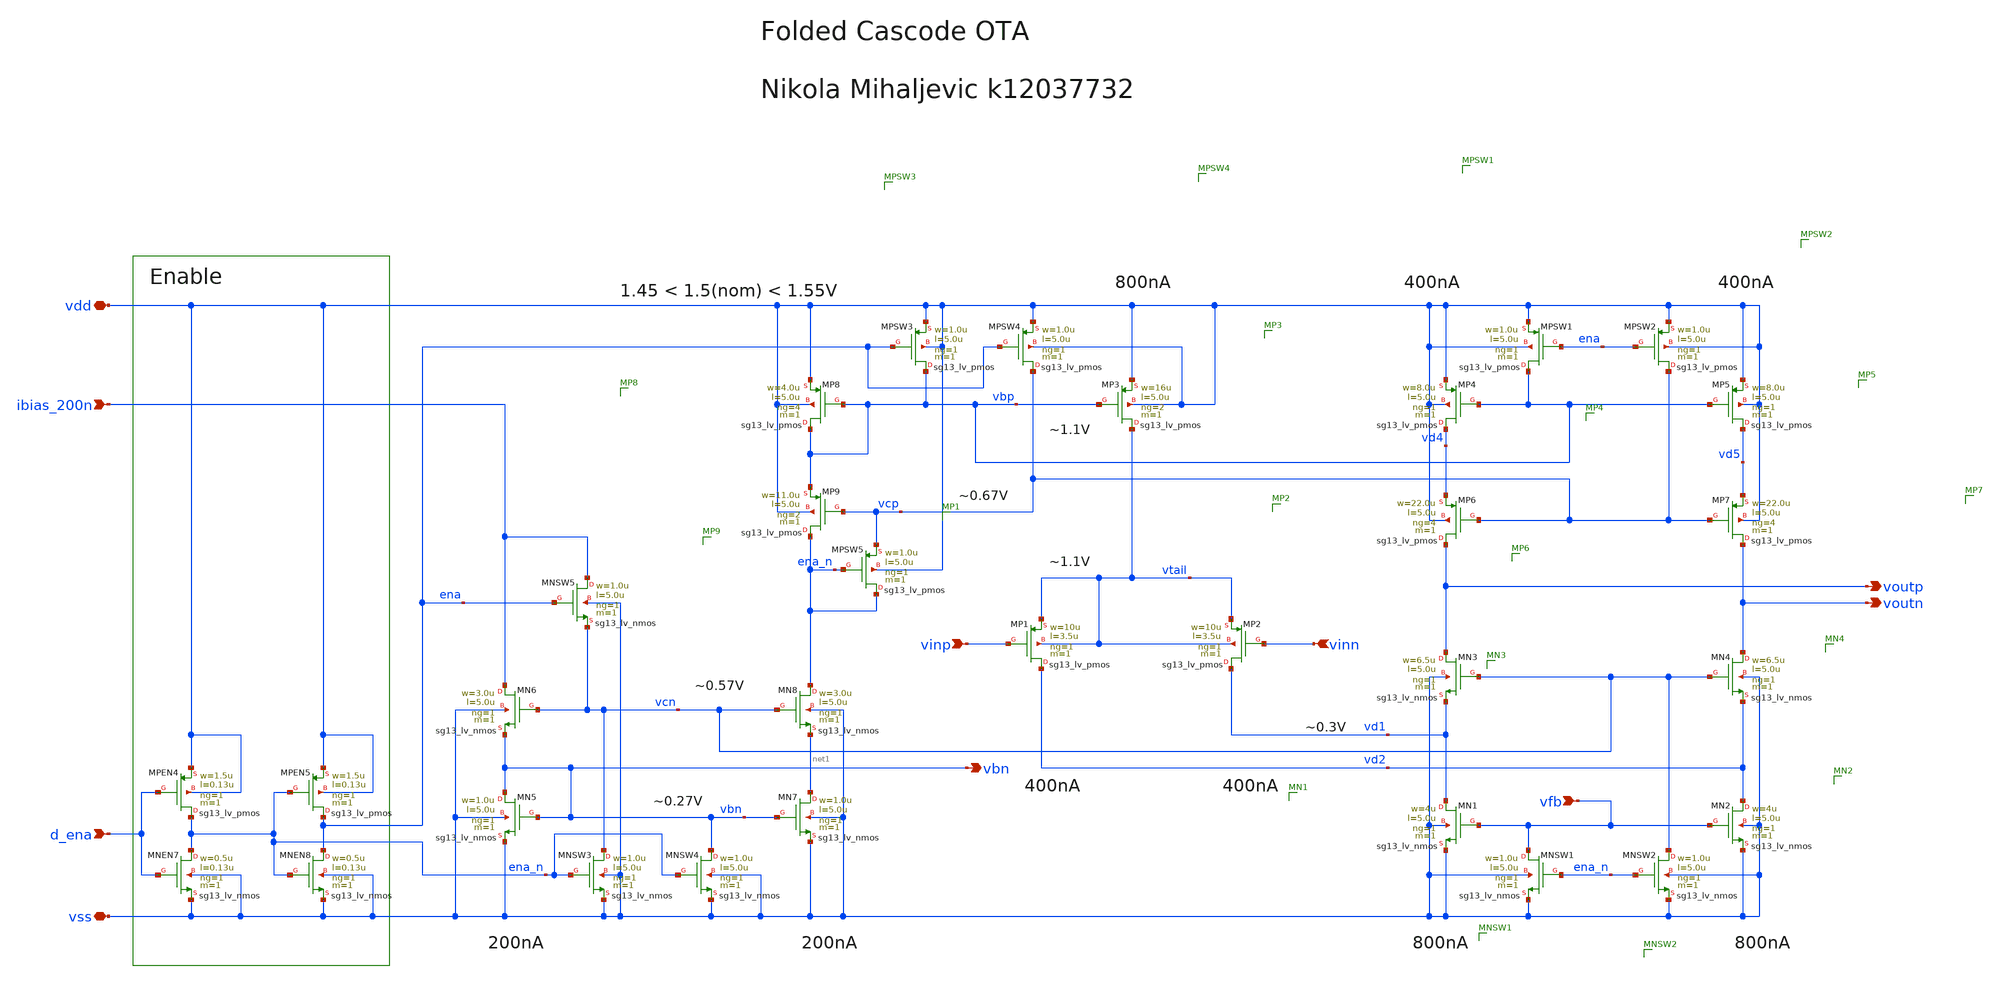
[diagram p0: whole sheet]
** sch_path: ota-fcasc-fd.sch
**.subckt ota-fcasc-fd ibias_200n vdd vss vinp vinn voutn d_ena voutp vfb vbn
*.ipin ibias_200n
*.iopin vdd
*.iopin vss
*.ipin vinp
*.ipin vinn
*.opin voutn
*.ipin d_ena
*.opin voutp
*.ipin vfb
*.opin vbn
XMN5 vbn vbn vss vss sg13_lv_nmos w=1.0u l=5.0u ng=1 m=1 mm_ok=1
XMNSW4 vbn ena_n vss vss sg13_lv_nmos w=1.0u l=5.0u ng=1 m=1 mm_ok=1
XMPSW1 vbp ena vdd vdd sg13_lv_pmos w=1.0u l=5.0u ng=1 m=1 mm_ok=1
XMNEN8 ena ena_n vss vss sg13_lv_nmos w=0.5u l=0.13u ng=1 m=1 mm_ok=1
XMPEN5 ena ena_n vdd vdd sg13_lv_pmos w=1.5u l=0.13u ng=1 m=1 mm_ok=1
XMNSW5 ibias_200n ena vcn vss sg13_lv_nmos w=1.0u l=5.0u ng=1 m=1 mm_ok=1
XMNEN7 ena_n d_ena vss vss sg13_lv_nmos w=0.5u l=0.13u ng=1 m=1 mm_ok=1
XMPEN4 ena_n d_ena vdd vdd sg13_lv_pmos w=1.5u l=0.13u ng=1 m=1 mm_ok=1
XMP1 vd2 vinp vtail vtail sg13_lv_pmos w=10u l=3.5u ng=1 m=1 mm_ok=1
XMP2 vd1 vinn vtail vtail sg13_lv_pmos w=10u l=3.5u ng=1 m=1 mm_ok=1
XMP3 vtail vbp vdd vdd sg13_lv_pmos w=16u l=5.0u ng=2 m=1 mm_ok=1
XMP6 voutp vcp vd4 vdd sg13_lv_pmos w=22.0u l=5.0u ng=4 m=1 mm_ok=1
XMP7 voutn vcp vd5 vdd sg13_lv_pmos w=22.0u l=5.0u ng=4 m=1 mm_ok=1
XMP4 vd4 vbp vdd vdd sg13_lv_pmos w=8.0u l=5.0u ng=1 m=1 mm_ok=1
XMP5 vd5 vbp vdd vdd sg13_lv_pmos w=8.0u l=5.0u ng=1 m=1 mm_ok=1
XMN3 voutp vcn vd1 vss sg13_lv_nmos w=6.5u l=5.0u ng=1 m=1 mm_ok=1
XMN4 voutn vcn vd2 vss sg13_lv_nmos w=6.5u l=5.0u ng=1 m=1 mm_ok=1
XMN1 vd1 vfb vss vss sg13_lv_nmos w=4u l=5.0u ng=1 m=1 mm_ok=1
XMN2 vd2 vfb vss vss sg13_lv_nmos w=4u l=5.0u ng=1 m=1 mm_ok=1
XMPSW2 vcp ena vdd vdd sg13_lv_pmos w=1.0u l=5.0u ng=1 m=1 mm_ok=1
XMNSW1 vfb ena_n vss vss sg13_lv_nmos w=1.0u l=5.0u ng=1 m=1 mm_ok=1
XMNSW2 vcn ena_n vss vss sg13_lv_nmos w=1.0u l=5.0u ng=1 m=1 mm_ok=1
XMN6 ibias_200n vcn vbn vss sg13_lv_nmos w=3.0u l=5.0u ng=1 m=1 mm_ok=1
XMN7 net1 vbn vss vss sg13_lv_nmos w=1.0u l=5.0u ng=1 m=1 mm_ok=1
XMN8 ena_n vcn net1 vss sg13_lv_nmos w=3.0u l=5.0u ng=1 m=1 mm_ok=1
XMP8 vbp vbp vdd vdd sg13_lv_pmos w=4.0u l=5.0u ng=4 m=1 mm_ok=1
XMP9 ena_n vcp vbp vdd sg13_lv_pmos w=11.0u l=5.0u ng=2 m=1 mm_ok=1
XMPSW3 vbp ena vdd vdd sg13_lv_pmos w=1.0u l=5.0u ng=1 m=1 mm_ok=1
XMPSW5 ena_n ena_n vcp vdd sg13_lv_pmos w=1.0u l=5.0u ng=1 m=1 mm_ok=1
XMNSW3 vcn ena_n vss vss sg13_lv_nmos w=1.0u l=5.0u ng=1 m=1 mm_ok=1
XMPSW4 vcp ena vdd vdd sg13_lv_pmos w=1.0u l=5.0u ng=1 m=1 mm_ok=1
**.ends
.end
